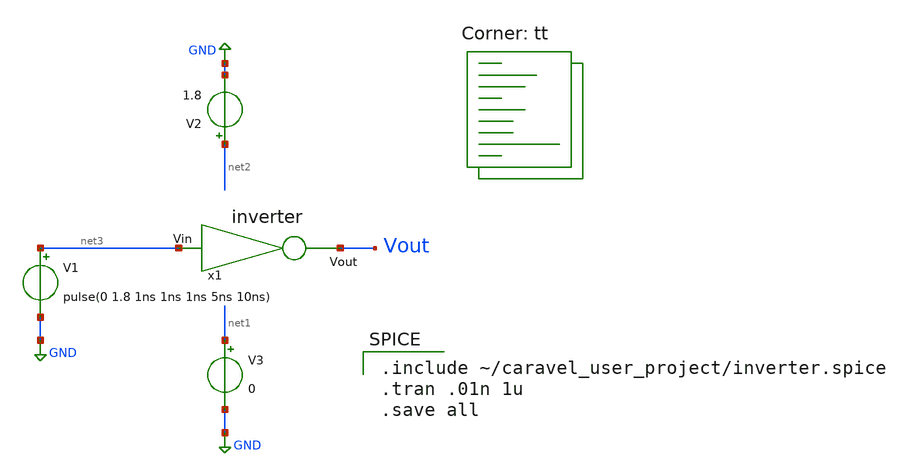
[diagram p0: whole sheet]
** sch_path: xschem/TestBenches/inverterTB.sch
**.subckt inverterTB
x1 Vout net3 inverter
V1 net3 GND pulse(0 1.8 1ns 1ns 1ns 5ns 10ns)
V2 net2 GND 1.8
V3 net1 GND 0
**** begin user architecture code

.include ~/caravel_user_project/inverter.spice
.tran .01n 1u
.save all

.lib $::SKYWATER_MODELS/sky130.lib.spice tt
**** end user architecture code
**.ends
.GLOBAL GND
.end
